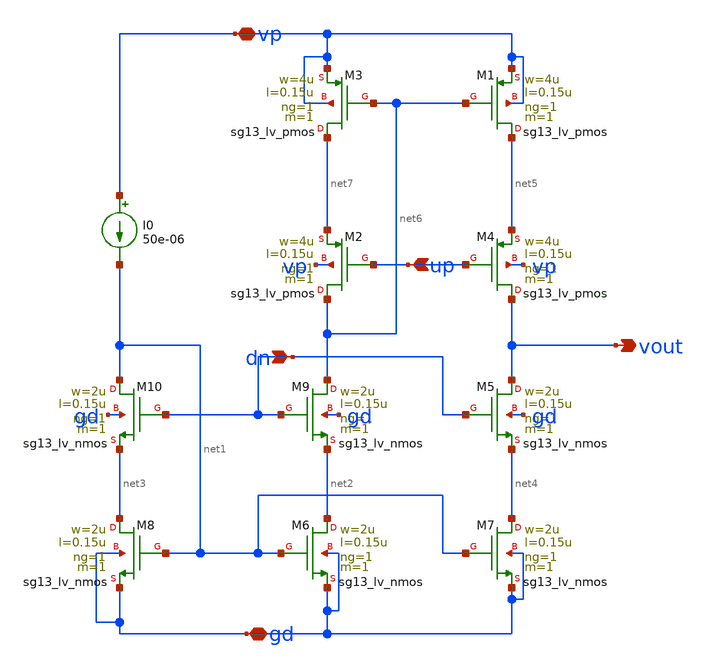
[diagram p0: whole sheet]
** sch_path: schematics/charge_pump/old_sch/cp_v4.sch
**.subckt cp_v4 up dn vout vp gd
*.ipin up
*.ipin dn
*.opin vout
*.iopin vp
*.iopin gd
XM3 net7 net6 vp vp sg13_lv_pmos w=4u l=0.15u ng=1 m=1 mm_ok=1
XM9 net6 dn net2 gd sg13_lv_nmos w=2u l=0.15u ng=1 m=1 mm_ok=1
XM1 net5 net6 vp vp sg13_lv_pmos w=4u l=0.15u ng=1 m=1 mm_ok=1
XM2 net6 up net7 vp sg13_lv_pmos w=4u l=0.15u ng=1 m=1 mm_ok=1
XM4 vout up net5 vp sg13_lv_pmos w=4u l=0.15u ng=1 m=1 mm_ok=1
XM5 vout dn net4 gd sg13_lv_nmos w=2u l=0.15u ng=1 m=1 mm_ok=1
XM6 net2 net1 gd gd sg13_lv_nmos w=2u l=0.15u ng=1 m=1 mm_ok=1
XM7 net4 net1 gd gd sg13_lv_nmos w=2u l=0.15u ng=1 m=1 mm_ok=1
XM8 net3 net1 gd gd sg13_lv_nmos w=2u l=0.15u ng=1 m=1 mm_ok=1
XM10 net1 dn net3 gd sg13_lv_nmos w=2u l=0.15u ng=1 m=1 mm_ok=1
I0 vp net1 50e-06
**.ends
.end
